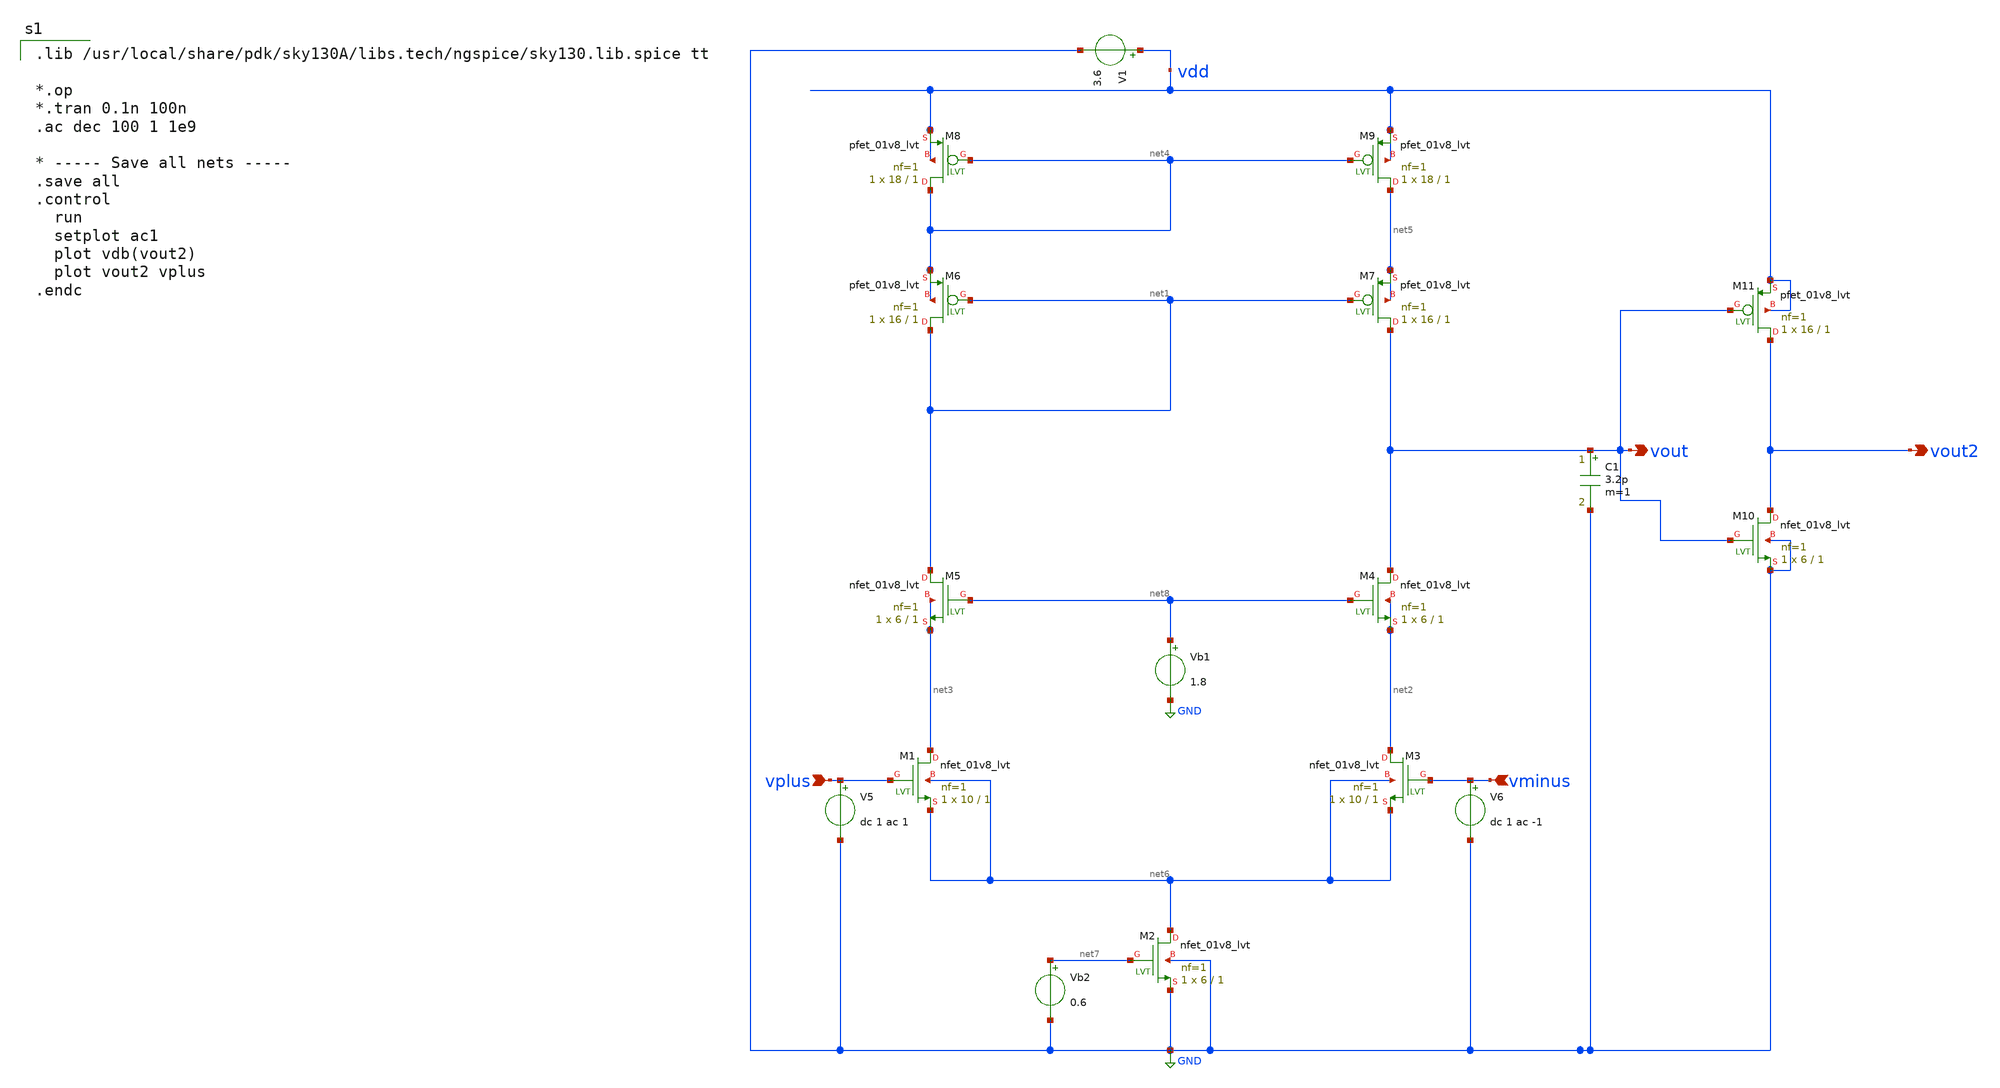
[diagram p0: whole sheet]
** sch_path: telescopic_2stg.sch
**.subckt telescopic_2stg vplus vminus vout vout2
*.ipin vplus
*.ipin vminus
*.opin vout
*.opin vout2
C1 vout GND 3.2p m=1
V1 vdd GND 3.6
Vb2 net7 GND 0.6
V5 vplus GND dc 1 ac 1
V6 vminus GND dc 1 ac -1
XM1 net3 vplus net6 net6 sky130_fd_pr__nfet_01v8_lvt L=1 W=10 nf=1 ad='int((1 + 1)/2) * 10 / 1 * 0.29'
+ as='int((1 + 2)/2) * 10 / 1 * 0.29' pd='2*int((1 + 1)/2) * (10 / 1 + 0.29)' ps='2*int((1 + 2)/2) * (10 / 1 + 0.29)'
+ nrd='0.29 / 10 ' nrs='0.29 / 10 ' sa=0 sb=0 sd=0 mult=1 m=1
XM2 net6 net7 GND GND sky130_fd_pr__nfet_01v8_lvt L=1 W=6 nf=1 ad='int((1 + 1)/2) * 6 / 1 * 0.29' as='int((1 + 2)/2) * 6 / 1 * 0.29'
+ pd='2*int((1 + 1)/2) * (6 / 1 + 0.29)' ps='2*int((1 + 2)/2) * (6 / 1 + 0.29)' nrd='0.29 / 6 ' nrs='0.29 / 6 '
+ sa=0 sb=0 sd=0 mult=1 m=1
XM3 net2 vminus net6 net6 sky130_fd_pr__nfet_01v8_lvt L=1 W=10 nf=1 ad='int((1 + 1)/2) * 10 / 1 * 0.29'
+ as='int((1 + 2)/2) * 10 / 1 * 0.29' pd='2*int((1 + 1)/2) * (10 / 1 + 0.29)' ps='2*int((1 + 2)/2) * (10 / 1 + 0.29)'
+ nrd='0.29 / 10 ' nrs='0.29 / 10 ' sa=0 sb=0 sd=0 mult=1 m=1
XM4 vout net8 net2 net2 sky130_fd_pr__nfet_01v8_lvt L=1 W=6 nf=1 ad='int((1 + 1)/2) * 6 / 1 * 0.29' as='int((1 + 2)/2) * 6 / 1 * 0.29'
+ pd='2*int((1 + 1)/2) * (6 / 1 + 0.29)' ps='2*int((1 + 2)/2) * (6 / 1 + 0.29)' nrd='0.29 / 6 ' nrs='0.29 / 6 '
+ sa=0 sb=0 sd=0 mult=1 m=1
XM5 net1 net8 net3 net3 sky130_fd_pr__nfet_01v8_lvt L=1 W=6 nf=1 ad='int((1 + 1)/2) * 6 / 1 * 0.29' as='int((1 + 2)/2) * 6 / 1 * 0.29'
+ pd='2*int((1 + 1)/2) * (6 / 1 + 0.29)' ps='2*int((1 + 2)/2) * (6 / 1 + 0.29)' nrd='0.29 / 6 ' nrs='0.29 / 6 '
+ sa=0 sb=0 sd=0 mult=1 m=1
XM6 net1 net1 net4 net4 sky130_fd_pr__pfet_01v8_lvt L=1 W=16 nf=1 ad='int((1 + 1)/2) * 16 / 1 * 0.29'
+ as='int((1 + 2)/2) * 16 / 1 * 0.29' pd='2*int((1 + 1)/2) * (16 / 1 + 0.29)' ps='2*int((1 + 2)/2) * (16 / 1 + 0.29)'
+ nrd='0.29 / 16 ' nrs='0.29 / 16 ' sa=0 sb=0 sd=0 mult=1 m=1
XM7 vout net1 net5 net5 sky130_fd_pr__pfet_01v8_lvt L=1 W=16 nf=1 ad='int((1 + 1)/2) * 16 / 1 * 0.29'
+ as='int((1 + 2)/2) * 16 / 1 * 0.29' pd='2*int((1 + 1)/2) * (16 / 1 + 0.29)' ps='2*int((1 + 2)/2) * (16 / 1 + 0.29)'
+ nrd='0.29 / 16 ' nrs='0.29 / 16 ' sa=0 sb=0 sd=0 mult=1 m=1
XM8 net4 net4 vdd vdd sky130_fd_pr__pfet_01v8_lvt L=1 W=18 nf=1 ad='int((1 + 1)/2) * 18 / 1 * 0.29' as='int((1 + 2)/2) * 18 / 1 * 0.29'
+ pd='2*int((1 + 1)/2) * (18 / 1 + 0.29)' ps='2*int((1 + 2)/2) * (18 / 1 + 0.29)' nrd='0.29 / 18 ' nrs='0.29 / 18 '
+ sa=0 sb=0 sd=0 mult=1 m=1
XM9 net5 net4 vdd vdd sky130_fd_pr__pfet_01v8_lvt L=1 W=18 nf=1 ad='int((1 + 1)/2) * 18 / 1 * 0.29' as='int((1 + 2)/2) * 18 / 1 * 0.29'
+ pd='2*int((1 + 1)/2) * (18 / 1 + 0.29)' ps='2*int((1 + 2)/2) * (18 / 1 + 0.29)' nrd='0.29 / 18 ' nrs='0.29 / 18 '
+ sa=0 sb=0 sd=0 mult=1 m=1
Vb1 net8 GND 1.8
XM10 vout2 vout GND GND sky130_fd_pr__nfet_01v8_lvt L=1 W=6 nf=1 ad='int((1 + 1)/2) * 6 / 1 * 0.29' as='int((1 + 2)/2) * 6 / 1 * 0.29'
+ pd='2*int((1 + 1)/2) * (6 / 1 + 0.29)' ps='2*int((1 + 2)/2) * (6 / 1 + 0.29)' nrd='0.29 / 6 ' nrs='0.29 / 6 '
+ sa=0 sb=0 sd=0 mult=1 m=1
XM11 vout2 vout vdd vdd sky130_fd_pr__pfet_01v8_lvt L=1 W=16 nf=1 ad='int((1 + 1)/2) * 16 / 1 * 0.29'
+ as='int((1 + 2)/2) * 16 / 1 * 0.29' pd='2*int((1 + 1)/2) * (16 / 1 + 0.29)' ps='2*int((1 + 2)/2) * (16 / 1 + 0.29)'
+ nrd='0.29 / 16 ' nrs='0.29 / 16 ' sa=0 sb=0 sd=0 mult=1 m=1
**** begin user architecture code

.lib /usr/local/share/pdk/sky130A/libs.tech/ngspice/sky130.lib.spice tt

*.op
*.tran 0.1n 100n
.ac dec 100 1 1e9

* ----- Save all nets -----
.save all
.control
  run
  setplot ac1
  plot vdb(vout2)
  plot vout2 vplus
.endc

**** end user architecture code
**.ends
.GLOBAL GND
.end
